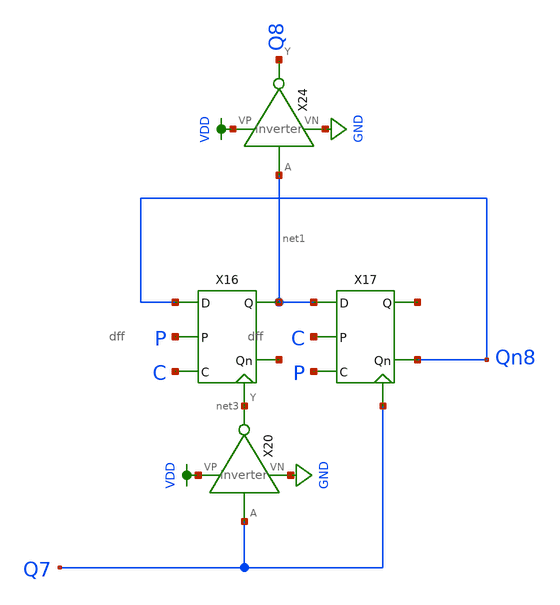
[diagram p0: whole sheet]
** sch_path: schematic/counter-bn_lvs.sch
**.subckt counter-bn_lvs
X16 Qn8 net2 net1 net3 P C dff
X17 net1 Qn8 net4 Q7 C P dff
X20 Q7 net3 VDD GND inverter
X24 net1 Q8 VDD GND inverter
**.ends
.GLOBAL VDD
.GLOBAL GND
.end
